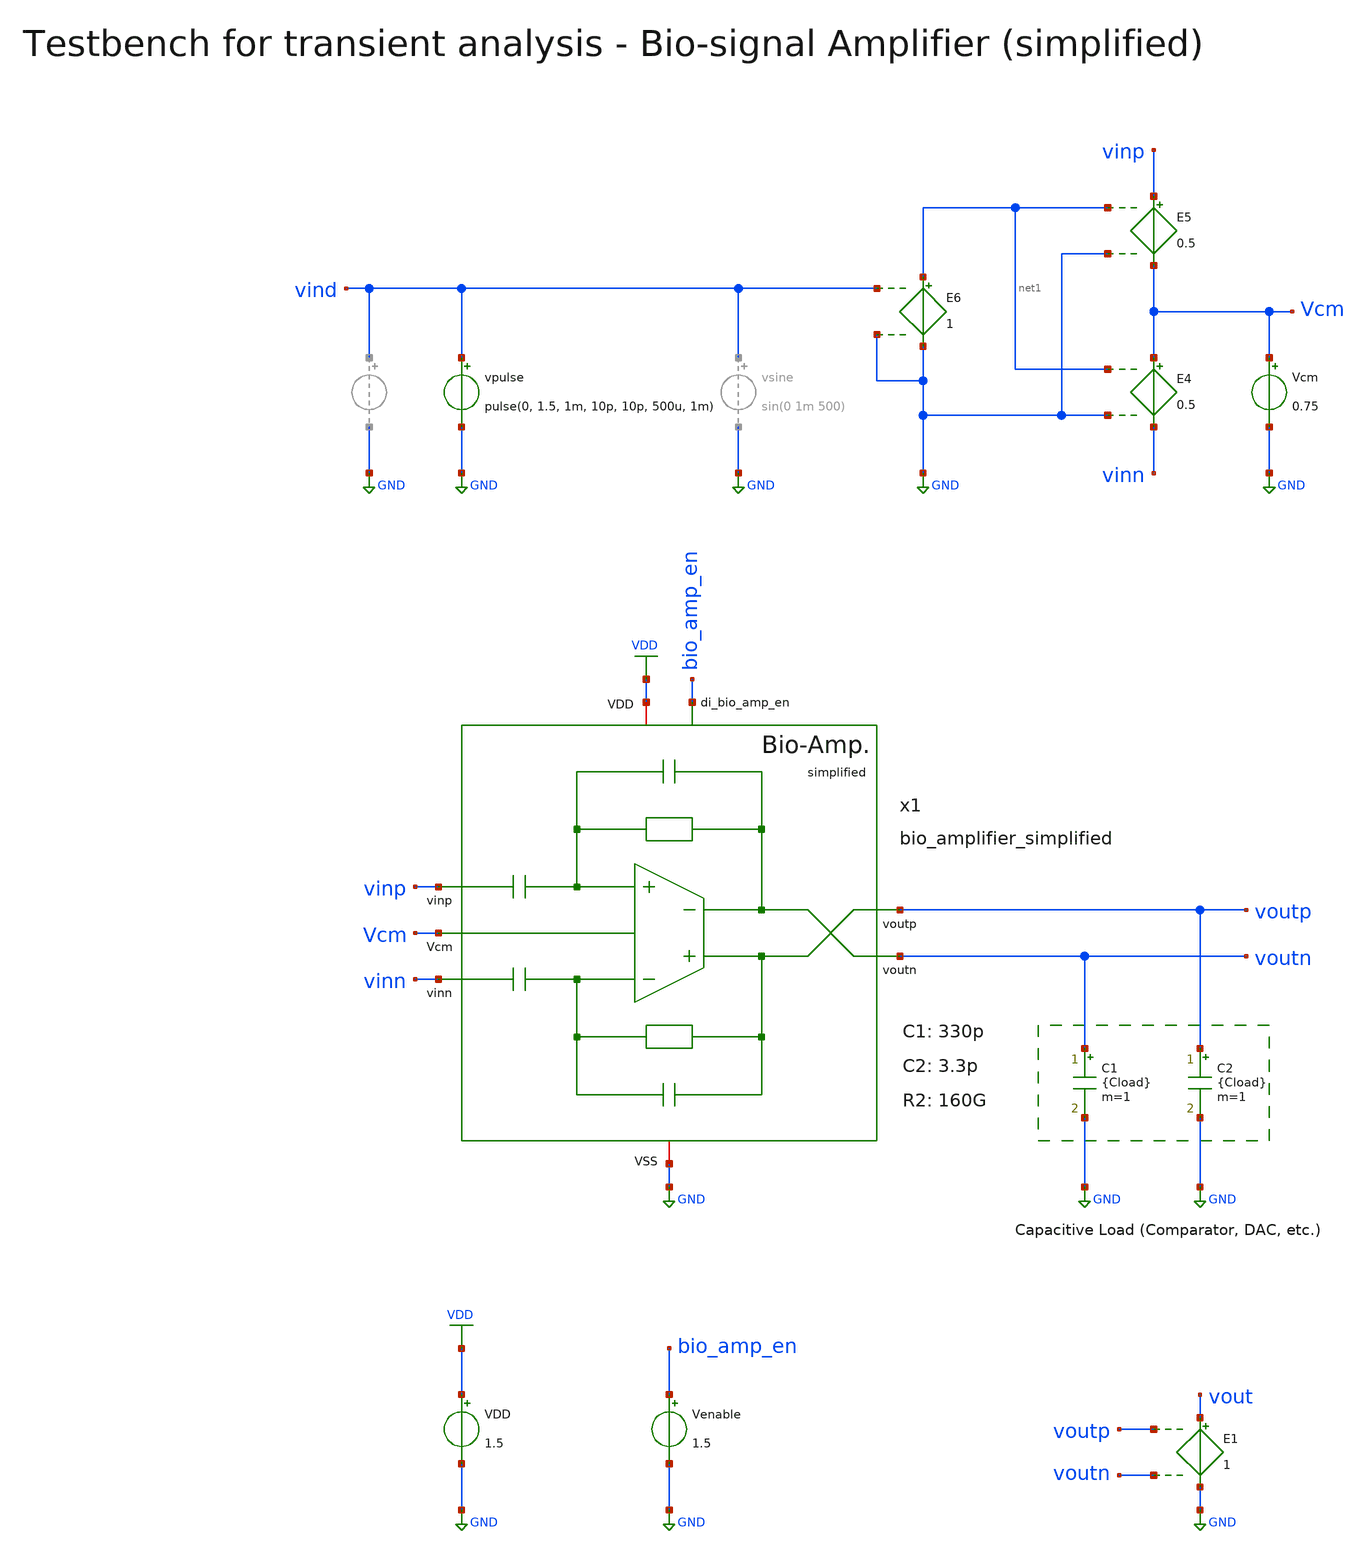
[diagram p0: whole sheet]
** sch_path: SG13G2_ATBS-ADC-main/xschem/bio_amplifier/testbenches/bio_amplifier_simplified_tb_tran.sch
**.subckt bio_amplifier_simplified_tb_tran
VDD VDD GND 1.5
C1 voutn GND {Cload} m=1
C2 voutp GND {Cload} m=1
Vcm Vcm GND 0.75
E4 Vcm vinn net1 GND 0.5
E5 vinp Vcm net1 GND 0.5
E6 net1 GND vind GND 1
E1 vout GND voutp voutn 1
vpulse vind GND pulse(0, 1.5, 1m, 10p, 10p, 500u, 1m)
x1 voutp bio_amp_en vinp Vcm voutn vinn VDD GND bio_amplifier_simplified C1=330p C2=3.3p R2=160G
Venable bio_amp_en GND 1.5
**** begin user architecture code

.lib cornerMOSlv.lib mos_tt
.lib cornerMOShv.lib mos_tt
.lib cornerRES.lib res_typ



.param temp=27
* 400fF DAC
.param Cload=227.56f
.options savecurrents klu method=gear reltol=1e-2 abstol=1e-15 gmin=1e-15 rshunt=1e12
.control

optran 0 0 0 1u 1m 0

save vind vinp vinn voutp voutn vout bio_amp_en x1.x1.Vbias x1.x1.Vbiasc x1.vinpa x1.vinna

* User Constants
let tstop = 2.5m

* Operating Point Analysis
op
remzerovec
write bio_amplifier_simplified_tb_tran.raw
set appendwrite

* Transient Analysis
tran 125n $&tstop

write bio_amplifier_simplified_tb_tran.raw

* Measurements
meas tran vin_peak MAX v(vind)
meas tran vout_peak MAX v(vout)

let Adm = vout_peak / vin_peak
let Adm_dB = vdb(Adm)
print Adm_dB

meas tran vout_pp_max MAX v(voutp)
meas tran vout_pp_min MIN v(voutp)
let vout_pp = vout_pp_max - vout_pp_min
print vout_pp

* Measure Settling Time of Output
* let voutp_limit = 0.6
* meas tran tcross WHEN v(voutp)=voutp_limit
* let ven_limit = 0.5 * 1.5
* meas tran tstart WHEN v(bio_amp_en)=ven_limit
* let tsettle = tcross - tstart
* print tsettle

* Calculate Power Consumption
* meas tran i_int INTEG i(VDD) from=0p to=tstop
* let power = 1.5 * i_int / tstop * 1e6
* echo Power Consumption $&power uW

* Plotting
plot vinp vinn voutp voutn bio_amp_en
plot vind vout
plot x1.vinpa x1.vinna voutp voutn
plot x1.x1.Vbias x1.x1.Vbiasc

* Write Data
set wr_vecnames
set wr_singlescale
let Vbias=x1.x1.Vbias
let Vbiasc=x1.x1.Vbiasc
wrdata
+ /foss/designs/SG13G2_ATBS-ADC-main/python/plot_simulations/data/bio_amplifier_simplified_tb_tran.txt v(vind) v(vinp) v(vinn) v(voutp) v(voutn) v(vout) v(Vbias) v(Vbiasc)

*quit
.endc


**** end user architecture code
**.ends
.GLOBAL GND
.GLOBAL VDD
.end
